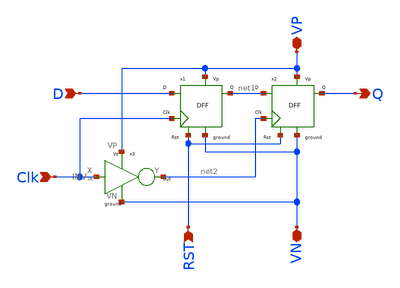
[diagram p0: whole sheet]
** sch_path: component/FlipFlops/MSFF.sch
**.subckt MSFF VP Clk RST Q D VN
*.iopin VP
*.ipin Clk
*.ipin RST
*.opin Q
*.ipin D
*.iopin VN
x1 D Clk RST VN VP net1 DFF
x2 net1 net2 RST VN VP Q DFF
x3 Clk net2 VP VN INV
**.ends

* expanding   symbol:  CCC/FlipFlops/DFF.sym # of pins=6
** sym_path: component/FlipFlops/DFF.sym
** sch_path: component/FlipFlops/DFF.sch
.subckt DFF D Clk RST VN VP Q
*.opin Q
*.iopin VN
*.iopin VP
*.ipin Clk
*.ipin D
*.ipin RST
x1 net2 net5 net4 VP VN NAND
x7 net4 Clk RST VP VN net2 NAND3
x3 Q net1 RST VP VN net3 NAND3
x4 net2 Clk net5 VP VN net1 NAND3
x5 net1 D RST VP VN net5 NAND3
x6 net3 net2 Q VP VN NAND
.ends


* expanding   symbol:  CCC/StdINV & RdnINV/INV.sym # of pins=4
** sym_path: component/INV/INV.sym
** sch_path: component/INV/INV.sch
.subckt INV X Y VP VN
*.ipin X
*.opin Y
*.iopin VN
*.iopin VP
XM1 Y X VN VN sky130_fd_pr__nfet_01v8 L=0.15 W=0.42 nf=1 ad='int((nf+1)/2) * W/nf * 0.29' as='int((nf+2)/2) * W/nf * 0.29'
+ pd='2*int((nf+1)/2) * (W/nf + 0.29)' ps='2*int((nf+2)/2) * (W/nf + 0.29)' nrd='0.29 / W' nrs='0.29 / W'
+ sa=0 sb=0 sd=0 mult=1 m=1
XM2 Y X VP VP sky130_fd_pr__pfet_01v8 L=0.15 W=1.26 nf=1 ad='int((nf+1)/2) * W/nf * 0.29' as='int((nf+2)/2) * W/nf * 0.29'
+ pd='2*int((nf+1)/2) * (W/nf + 0.29)' ps='2*int((nf+2)/2) * (W/nf + 0.29)' nrd='0.29 / W' nrs='0.29 / W'
+ sa=0 sb=0 sd=0 mult=1 m=1
.ends


* expanding   symbol:  component/NAND2/NAND.sym # of pins=5
** sym_path: component/NAND2/NAND.sym
** sch_path: component/NAND2/NAND.sch
.subckt NAND B A Y VP VN
*.iopin VP
*.ipin A
*.ipin B
*.opin Y
*.iopin VN
XM1 Y A VP VP sky130_fd_pr__pfet_01v8 L=0.15 W=1.26 nf=1 ad='int((nf+1)/2) * W/nf * 0.29' as='int((nf+2)/2) * W/nf * 0.29'
+ pd='2*int((nf+1)/2) * (W/nf + 0.29)' ps='2*int((nf+2)/2) * (W/nf + 0.29)' nrd='0.29 / W' nrs='0.29 / W'
+ sa=0 sb=0 sd=0 mult=1 m=1
XM2 Y B VP VP sky130_fd_pr__pfet_01v8 L=0.15 W=1.26 nf=1 ad='int((nf+1)/2) * W/nf * 0.29' as='int((nf+2)/2) * W/nf * 0.29'
+ pd='2*int((nf+1)/2) * (W/nf + 0.29)' ps='2*int((nf+2)/2) * (W/nf + 0.29)' nrd='0.29 / W' nrs='0.29 / W'
+ sa=0 sb=0 sd=0 mult=1 m=1
XM3 Y A net1 net1 sky130_fd_pr__nfet_01v8 L=0.15 W=0.84 nf=1 ad='int((nf+1)/2) * W/nf * 0.29' as='int((nf+2)/2) * W/nf * 0.29'
+ pd='2*int((nf+1)/2) * (W/nf + 0.29)' ps='2*int((nf+2)/2) * (W/nf + 0.29)' nrd='0.29 / W' nrs='0.29 / W'
+ sa=0 sb=0 sd=0 mult=1 m=1
XM4 net1 B VN VN sky130_fd_pr__nfet_01v8 L=0.15 W=0.84 nf=1 ad='int((nf+1)/2) * W/nf * 0.29' as='int((nf+2)/2) * W/nf * 0.29'
+ pd='2*int((nf+1)/2) * (W/nf + 0.29)' ps='2*int((nf+2)/2) * (W/nf + 0.29)' nrd='0.29 / W' nrs='0.29 / W'
+ sa=0 sb=0 sd=0 mult=1 m=1
.ends


* expanding   symbol:  component/NAND3/NAND3.sym # of pins=6
** sym_path: component/NAND3/NAND3.sym
** sch_path: component/NAND3/NAND3.sch
.subckt NAND3 A B C VP VN Y
*.iopin VP
*.iopin VN
*.ipin A
*.ipin B
*.ipin C
*.opin Y
XM1 Y A net1 VN sky130_fd_pr__nfet_01v8 L=0.15 W=1.26 nf=1 ad='int((nf+1)/2) * W/nf * 0.29' as='int((nf+2)/2) * W/nf * 0.29'
+ pd='2*int((nf+1)/2) * (W/nf + 0.29)' ps='2*int((nf+2)/2) * (W/nf + 0.29)' nrd='0.29 / W' nrs='0.29 / W'
+ sa=0 sb=0 sd=0 mult=1 m=1
XM2 net1 B net2 VN sky130_fd_pr__nfet_01v8 L=0.15 W=1.26 nf=1 ad='int((nf+1)/2) * W/nf * 0.29' as='int((nf+2)/2) * W/nf * 0.29'
+ pd='2*int((nf+1)/2) * (W/nf + 0.29)' ps='2*int((nf+2)/2) * (W/nf + 0.29)' nrd='0.29 / W' nrs='0.29 / W'
+ sa=0 sb=0 sd=0 mult=1 m=1
XM3 net2 C VN VN sky130_fd_pr__nfet_01v8 L=0.15 W=1.26 nf=1 ad='int((nf+1)/2) * W/nf * 0.29' as='int((nf+2)/2) * W/nf * 0.29'
+ pd='2*int((nf+1)/2) * (W/nf + 0.29)' ps='2*int((nf+2)/2) * (W/nf + 0.29)' nrd='0.29 / W' nrs='0.29 / W'
+ sa=0 sb=0 sd=0 mult=1 m=1
XM4 Y A VP VP sky130_fd_pr__pfet_01v8 L=0.15 W=1.26 nf=1 ad='int((nf+1)/2) * W/nf * 0.29' as='int((nf+2)/2) * W/nf * 0.29'
+ pd='2*int((nf+1)/2) * (W/nf + 0.29)' ps='2*int((nf+2)/2) * (W/nf + 0.29)' nrd='0.29 / W' nrs='0.29 / W'
+ sa=0 sb=0 sd=0 mult=1 m=1
XM5 Y B VP VP sky130_fd_pr__pfet_01v8 L=0.15 W=1.26 nf=1 ad='int((nf+1)/2) * W/nf * 0.29' as='int((nf+2)/2) * W/nf * 0.29'
+ pd='2*int((nf+1)/2) * (W/nf + 0.29)' ps='2*int((nf+2)/2) * (W/nf + 0.29)' nrd='0.29 / W' nrs='0.29 / W'
+ sa=0 sb=0 sd=0 mult=1 m=1
XM6 Y C VP VP sky130_fd_pr__pfet_01v8 L=0.15 W=1.26 nf=1 ad='int((nf+1)/2) * W/nf * 0.29' as='int((nf+2)/2) * W/nf * 0.29'
+ pd='2*int((nf+1)/2) * (W/nf + 0.29)' ps='2*int((nf+2)/2) * (W/nf + 0.29)' nrd='0.29 / W' nrs='0.29 / W'
+ sa=0 sb=0 sd=0 mult=1 m=1
.ends

.end
